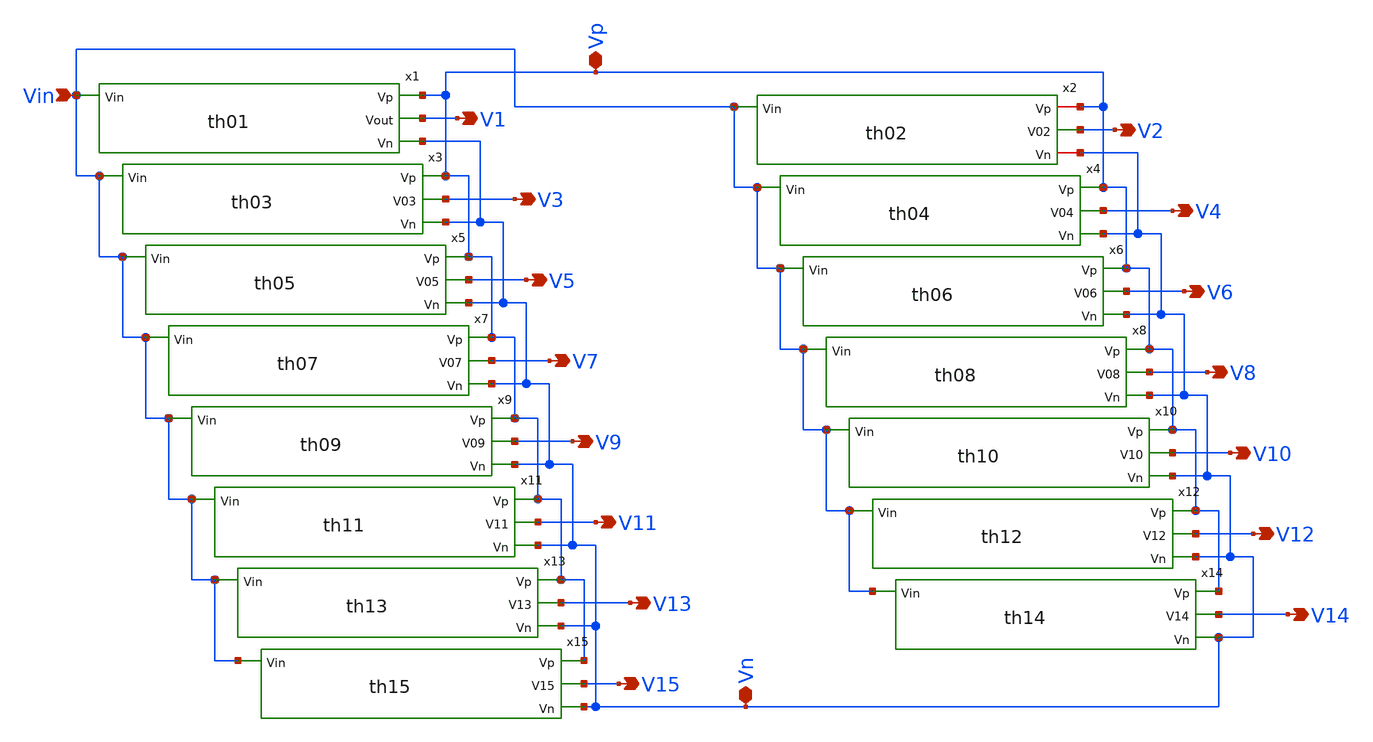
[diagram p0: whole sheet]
** sch_path: xschem/Vth_sch/Symbol/Analog.sch
**.subckt Analog Vin V1 V3 V5 V7 V9 V11 V13 V15 V2 V4 V6 V8 V10 V12 V14 Vp Vn
*.ipin Vin
*.opin V1
*.opin V3
*.opin V5
*.opin V7
*.opin V9
*.opin V11
*.opin V13
*.opin V15
*.opin V2
*.opin V4
*.opin V6
*.opin V8
*.opin V10
*.opin V12
*.opin V14
*.iopin Vp
*.iopin Vn
x1 Vp Vin V1 Vn th01
x2 Vp Vin V2 Vn th02
x3 Vp V3 Vin Vn th03
x4 Vp V4 Vin Vn th04
x5 Vp V5 Vin Vn th05
x6 Vp Vin V6 Vn th06
x7 Vp Vin V7 Vn th07
x8 Vp V8 Vin Vn th08
x9 Vp V9 Vin Vn th09
x10 Vp V10 Vin Vn th10
x11 Vp V11 Vin Vn th11
x12 Vp V12 Vin Vn th12
x13 Vp V13 Vin Vn th13
x14 Vp V14 Vin Vn th14
x15 Vp V15 Vin Vn th15
**.ends
.end
